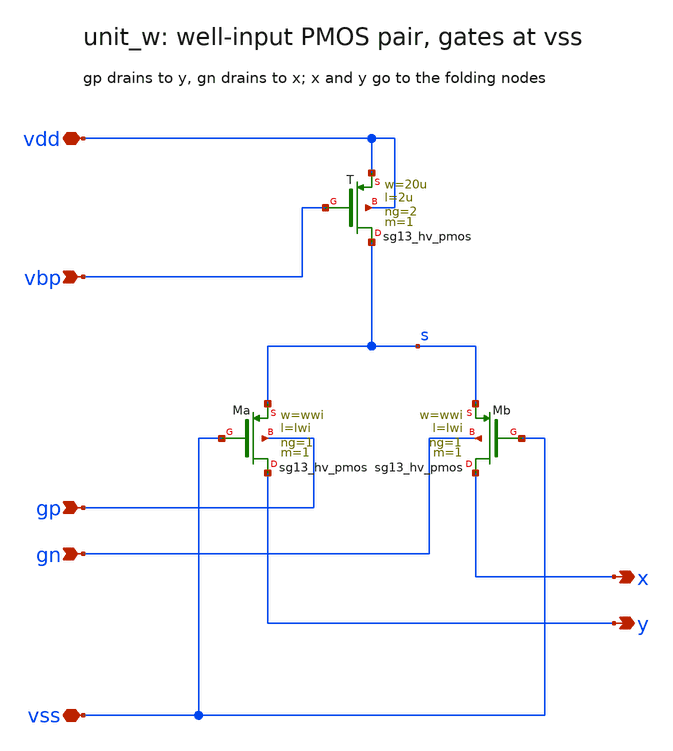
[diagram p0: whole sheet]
** sch_path: sudelbuecher/design_considerations/class_ab_pad_driver/improvements/xschem/unit_w.sch
**.subckt unit_w x y gp gn vdd vss vbp
*.opin x
*.opin y
*.ipin gp
*.ipin gn
*.iopin vdd
*.iopin vss
*.ipin vbp
XT s vbp vdd vdd sg13_hv_pmos w=20u l=2u ng=2 m=1 mm_ok=1
XMa y vss s gp sg13_hv_pmos w=wwi l=lwi ng=1 m=1 mm_ok=1
XMb x vss s gn sg13_hv_pmos w=wwi l=lwi ng=1 m=1 mm_ok=1
**.ends
.end
